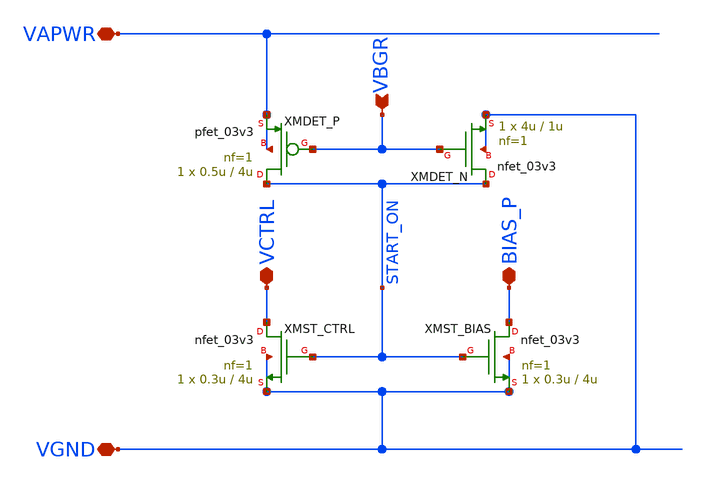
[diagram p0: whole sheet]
** sch_path: xschem/bgr_startup.sch
**.subckt bgr_startup VAPWR VGND VBGR BIAS_P VCTRL
*.iopin VAPWR
*.iopin VGND
*.ipin VBGR
*.iopin BIAS_P
*.iopin VCTRL
XMDET_N START_ON VBGR VGND VGND nfet_03v3 L=1u W=4u nf=1 ad='int((nf+1)/2) * W/nf * 0.18u' as='int((nf+2)/2) * W/nf * 0.18u'
+ pd='2*int((nf+1)/2) * (W/nf + 0.18u)' ps='2*int((nf+2)/2) * (W/nf + 0.18u)' nrd='0.18u / W' nrs='0.18u / W'
+ sa=0 sb=0 sd=0 m=1
XMST_BIAS BIAS_P START_ON VGND VGND nfet_03v3 L=4u W=0.3u nf=1 ad='int((nf+1)/2) * W/nf * 0.18u' as='int((nf+2)/2) * W/nf * 0.18u'
+ pd='2*int((nf+1)/2) * (W/nf + 0.18u)' ps='2*int((nf+2)/2) * (W/nf + 0.18u)' nrd='0.18u / W' nrs='0.18u / W'
+ sa=0 sb=0 sd=0 m=1
XMST_CTRL VCTRL START_ON VGND VGND nfet_03v3 L=4u W=0.3u nf=1 ad='int((nf+1)/2) * W/nf * 0.18u' as='int((nf+2)/2) * W/nf * 0.18u'
+ pd='2*int((nf+1)/2) * (W/nf + 0.18u)' ps='2*int((nf+2)/2) * (W/nf + 0.18u)' nrd='0.18u / W' nrs='0.18u / W'
+ sa=0 sb=0 sd=0 m=1
XMDET_P START_ON VBGR VAPWR VAPWR pfet_03v3 L=4u W=0.5u nf=1 ad='int((nf+1)/2) * W/nf * 0.18u' as='int((nf+2)/2) * W/nf * 0.18u'
+ pd='2*int((nf+1)/2) * (W/nf + 0.18u)' ps='2*int((nf+2)/2) * (W/nf + 0.18u)' nrd='0.18u / W' nrs='0.18u / W'
+ sa=0 sb=0 sd=0 m=1
**.ends
.end
